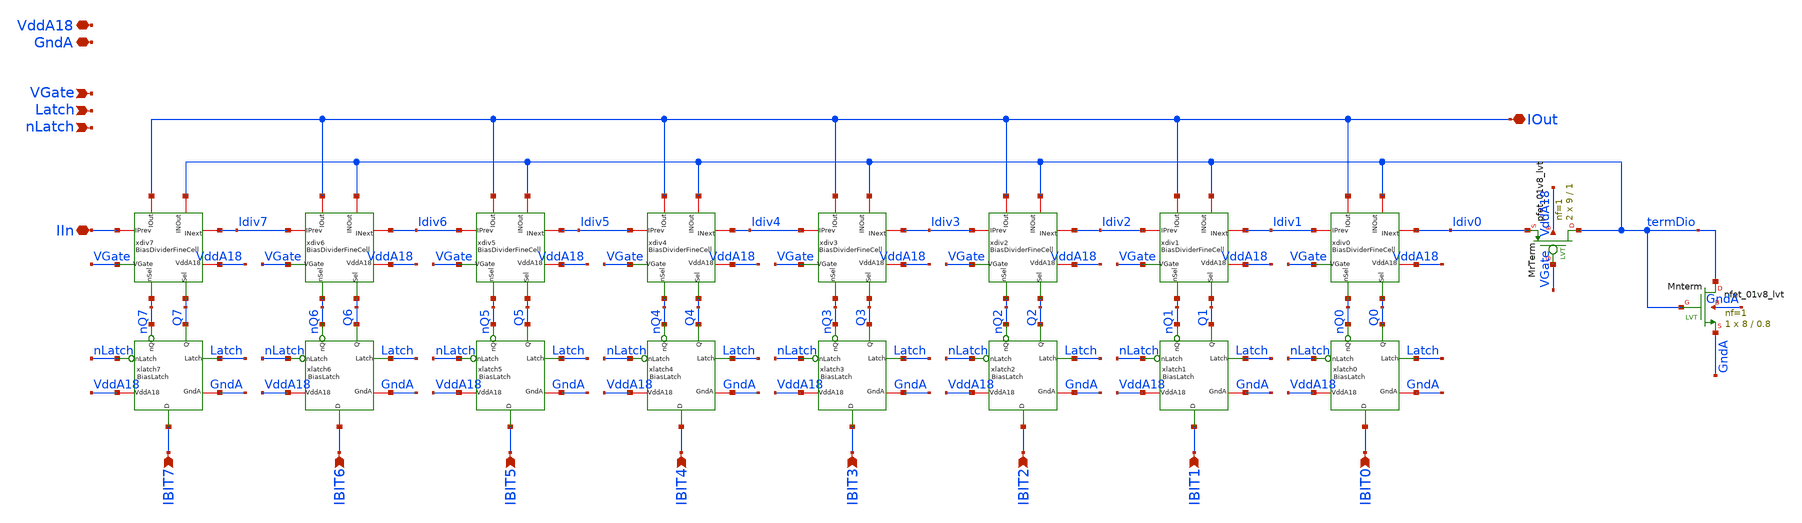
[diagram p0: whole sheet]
** sch_path: analog/xschem/BiasDividerFine.sch
**.subckt BiasDividerFine VddA18 GndA IBIT0 IBIT1 IBIT3 IOut IBIT2 IBIT4 IBIT5 IBIT7 IBIT6 VGate IIn
*+ Latch nLatch
*.iopin VddA18
*.iopin GndA
*.ipin IBIT0
*.ipin IBIT1
*.ipin IBIT3
*.iopin IOut
*.ipin IBIT2
*.ipin IBIT4
*.ipin IBIT5
*.ipin IBIT7
*.ipin IBIT6
*.ipin VGate
*.iopin IIn
*.ipin Latch
*.ipin nLatch
xdiv0 Idiv1 Idiv0 VGate IOut VddA18 termDio nQ0 Q0 BiasDividerFineCell
xlatch0 VddA18 GndA nQ0 Q0 Latch nLatch IBIT0 BiasLatch
xdiv1 Idiv2 Idiv1 VGate IOut VddA18 termDio nQ1 Q1 BiasDividerFineCell
xlatch1 VddA18 GndA nQ1 Q1 Latch nLatch IBIT1 BiasLatch
xdiv2 Idiv3 Idiv2 VGate IOut VddA18 termDio nQ2 Q2 BiasDividerFineCell
xlatch2 VddA18 GndA nQ2 Q2 Latch nLatch IBIT2 BiasLatch
xdiv3 Idiv4 Idiv3 VGate IOut VddA18 termDio nQ3 Q3 BiasDividerFineCell
xlatch3 VddA18 GndA nQ3 Q3 Latch nLatch IBIT3 BiasLatch
xdiv4 Idiv5 Idiv4 VGate IOut VddA18 termDio nQ4 Q4 BiasDividerFineCell
xlatch4 VddA18 GndA nQ4 Q4 Latch nLatch IBIT4 BiasLatch
xdiv5 Idiv6 Idiv5 VGate IOut VddA18 termDio nQ5 Q5 BiasDividerFineCell
xlatch5 VddA18 GndA nQ5 Q5 Latch nLatch IBIT5 BiasLatch
xdiv6 Idiv7 Idiv6 VGate IOut VddA18 termDio nQ6 Q6 BiasDividerFineCell
xlatch6 VddA18 GndA nQ6 Q6 Latch nLatch IBIT6 BiasLatch
xdiv7 IIn Idiv7 VGate IOut VddA18 termDio nQ7 Q7 BiasDividerFineCell
xlatch7 VddA18 GndA nQ7 Q7 Latch nLatch IBIT7 BiasLatch
XMrTerm termDio VGate Idiv0 VddA18 sky130_fd_pr__pfet_01v8_lvt L=1 W=9 nf=1 ad='int((1 + 1)/2) * 9 / 1 * 0.29'
+ as='int((1 + 2)/2) * 9 / 1 * 0.29' pd='2*int((1 + 1)/2) * (9 / 1 + 0.29)' ps='2*int((1 + 2)/2) * (9 / 1 + 0.29)'
+ nrd='0.29 / 9 ' nrs='0.29 / 9 ' sa=0 sb=0 sd=0 mult=2 m=2
XMnterm termDio termDio GndA GndA sky130_fd_pr__nfet_01v8_lvt L=0.8 W=8 nf=1 ad='int((1 + 1)/2) * 8 / 1 * 0.29'
+ as='int((1 + 2)/2) * 8 / 1 * 0.29' pd='2*int((1 + 1)/2) * (8 / 1 + 0.29)' ps='2*int((1 + 2)/2) * (8 / 1 + 0.29)'
+ nrd='0.29 / 8 ' nrs='0.29 / 8 ' sa=0 sb=0 sd=0 mult=1 m=1
**.ends

* expanding   symbol:  BiasDividerFineCell.sym # of pins=8
** sym_path: analog/xschem/BiasDividerFineCell.sym
** sch_path: analog/xschem/BiasDividerFineCell.sch
.subckt BiasDividerFineCell IPrev INext VGate IOut VddA18 INOut nSel Sel
*.iopin INext
*.iopin IOut
*.iopin IPrev
*.ipin VGate
*.iopin VddA18
*.ipin nSel
*.ipin Sel
*.iopin INOut
XMr INext VGate IPrev VddA18 sky130_fd_pr__pfet_01v8 L=1 W=9 nf=1 ad='int((1 + 1)/2) * 9 / 1 * 0.29'
+ as='int((1 + 2)/2) * 9 / 1 * 0.29' pd='2*int((1 + 1)/2) * (9 / 1 + 0.29)' ps='2*int((1 + 2)/2) * (9 / 1 + 0.29)'
+ nrd='0.29 / 9 ' nrs='0.29 / 9 ' sa=0 sb=0 sd=0 mult=2 m=2
XM2ru net1 VGate IPrev VddA18 sky130_fd_pr__pfet_01v8 L=1 W=9 nf=1 ad='int((1 + 1)/2) * 9 / 1 * 0.29'
+ as='int((1 + 2)/2) * 9 / 1 * 0.29' pd='2*int((1 + 1)/2) * (9 / 1 + 0.29)' ps='2*int((1 + 2)/2) * (9 / 1 + 0.29)'
+ nrd='0.29 / 9 ' nrs='0.29 / 9 ' sa=0 sb=0 sd=0 mult=2 m=2
XM2rl net2 VGate net1 VddA18 sky130_fd_pr__pfet_01v8 L=1 W=9 nf=1 ad='int((1 + 1)/2) * 9 / 1 * 0.29'
+ as='int((1 + 2)/2) * 9 / 1 * 0.29' pd='2*int((1 + 1)/2) * (9 / 1 + 0.29)' ps='2*int((1 + 2)/2) * (9 / 1 + 0.29)'
+ nrd='0.29 / 9 ' nrs='0.29 / 9 ' sa=0 sb=0 sd=0 mult=2 m=2
XMswNOut INOut Sel net2 VddA18 sky130_fd_pr__pfet_01v8 L=0.5 W=2 nf=1 ad='int((1 + 1)/2) * 2 / 1 * 0.29'
+ as='int((1 + 2)/2) * 2 / 1 * 0.29' pd='2*int((1 + 1)/2) * (2 / 1 + 0.29)' ps='2*int((1 + 2)/2) * (2 / 1 + 0.29)'
+ nrd='0.29 / 2 ' nrs='0.29 / 2 ' sa=0 sb=0 sd=0 mult=1 m=1
XMswOut IOut nSel net2 VddA18 sky130_fd_pr__pfet_01v8 L=0.5 W=2 nf=1 ad='int((1 + 1)/2) * 2 / 1 * 0.29'
+ as='int((1 + 2)/2) * 2 / 1 * 0.29' pd='2*int((1 + 1)/2) * (2 / 1 + 0.29)' ps='2*int((1 + 2)/2) * (2 / 1 + 0.29)'
+ nrd='0.29 / 2 ' nrs='0.29 / 2 ' sa=0 sb=0 sd=0 mult=1 m=1
.ends


* expanding   symbol:  BiasLatch.sym # of pins=7
** sym_path: analog/xschem/BiasLatch.sym
** sch_path: analog/xschem/BiasLatch.sch
.subckt BiasLatch VddA18 GndA nQ Q Latch nLatch D
*.ipin D
*.ipin Latch
*.ipin nLatch
*.opin Q
*.iopin GndA
*.iopin VddA18
*.opin nQ
XMnsw1 int nLatch D GndA sky130_fd_pr__nfet_01v8 L=0.15 W=0.42 nf=1 ad='int((1 + 1)/2) * 0.42 / 1 * 0.29'
+ as='int((1 + 2)/2) * 0.42 / 1 * 0.29' pd='2*int((1 + 1)/2) * (0.42 / 1 + 0.29)' ps='2*int((1 + 2)/2) * (0.42 / 1 + 0.29)'
+ nrd='0.29 / 0.42 ' nrs='0.29 / 0.42 ' sa=0 sb=0 sd=0 mult=1 m=1
XMpsw1 int Latch D VddA18 sky130_fd_pr__pfet_01v8_hvt L=0.15 W=0.42 nf=1 ad='int((1 + 1)/2) * 0.42 / 1 * 0.29'
+ as='int((1 + 2)/2) * 0.42 / 1 * 0.29' pd='2*int((1 + 1)/2) * (0.42 / 1 + 0.29)' ps='2*int((1 + 2)/2) * (0.42 / 1 + 0.29)'
+ nrd='0.29 / 0.42 ' nrs='0.29 / 0.42 ' sa=0 sb=0 sd=0 mult=1 m=1
XMnsw2 Q Latch int GndA sky130_fd_pr__nfet_01v8 L=0.15 W=0.42 nf=1 ad='int((1 + 1)/2) * 0.42 / 1 * 0.29'
+ as='int((1 + 2)/2) * 0.42 / 1 * 0.29' pd='2*int((1 + 1)/2) * (0.42 / 1 + 0.29)' ps='2*int((1 + 2)/2) * (0.42 / 1 + 0.29)'
+ nrd='0.29 / 0.42 ' nrs='0.29 / 0.42 ' sa=0 sb=0 sd=0 mult=1 m=1
XMpsw2 Q nLatch int VddA18 sky130_fd_pr__pfet_01v8_hvt L=0.15 W=0.42 nf=1 ad='int((1 + 1)/2) * 0.42 / 1 * 0.29'
+ as='int((1 + 2)/2) * 0.42 / 1 * 0.29' pd='2*int((1 + 1)/2) * (0.42 / 1 + 0.29)' ps='2*int((1 + 2)/2) * (0.42 / 1 + 0.29)'
+ nrd='0.29 / 0.42 ' nrs='0.29 / 0.42 ' sa=0 sb=0 sd=0 mult=1 m=1
XMpinv1 nQ int VddA18 VddA18 sky130_fd_pr__pfet_01v8_hvt L=0.15 W=0.42 nf=1 ad='int((1 + 1)/2) * 0.42 / 1 * 0.29'
+ as='int((1 + 2)/2) * 0.42 / 1 * 0.29' pd='2*int((1 + 1)/2) * (0.42 / 1 + 0.29)' ps='2*int((1 + 2)/2) * (0.42 / 1 + 0.29)'
+ nrd='0.29 / 0.42 ' nrs='0.29 / 0.42 ' sa=0 sb=0 sd=0 mult=1 m=1
XMpinv2 Q nQ VddA18 VddA18 sky130_fd_pr__pfet_01v8_hvt L=0.15 W=0.42 nf=1 ad='int((1 + 1)/2) * 0.42 / 1 * 0.29'
+ as='int((1 + 2)/2) * 0.42 / 1 * 0.29' pd='2*int((1 + 1)/2) * (0.42 / 1 + 0.29)' ps='2*int((1 + 2)/2) * (0.42 / 1 + 0.29)'
+ nrd='0.29 / 0.42 ' nrs='0.29 / 0.42 ' sa=0 sb=0 sd=0 mult=1 m=1
XMninv1 nQ int GndA GndA sky130_fd_pr__nfet_01v8 L=0.15 W=0.42 nf=1 ad='int((1 + 1)/2) * 0.42 / 1 * 0.29'
+ as='int((1 + 2)/2) * 0.42 / 1 * 0.29' pd='2*int((1 + 1)/2) * (0.42 / 1 + 0.29)' ps='2*int((1 + 2)/2) * (0.42 / 1 + 0.29)'
+ nrd='0.29 / 0.42 ' nrs='0.29 / 0.42 ' sa=0 sb=0 sd=0 mult=1 m=1
XMninv2 Q nQ GndA GndA sky130_fd_pr__nfet_01v8 L=0.15 W=0.42 nf=1 ad='int((1 + 1)/2) * 0.42 / 1 * 0.29'
+ as='int((1 + 2)/2) * 0.42 / 1 * 0.29' pd='2*int((1 + 1)/2) * (0.42 / 1 + 0.29)' ps='2*int((1 + 2)/2) * (0.42 / 1 + 0.29)'
+ nrd='0.29 / 0.42 ' nrs='0.29 / 0.42 ' sa=0 sb=0 sd=0 mult=1 m=1
.ends

.end
